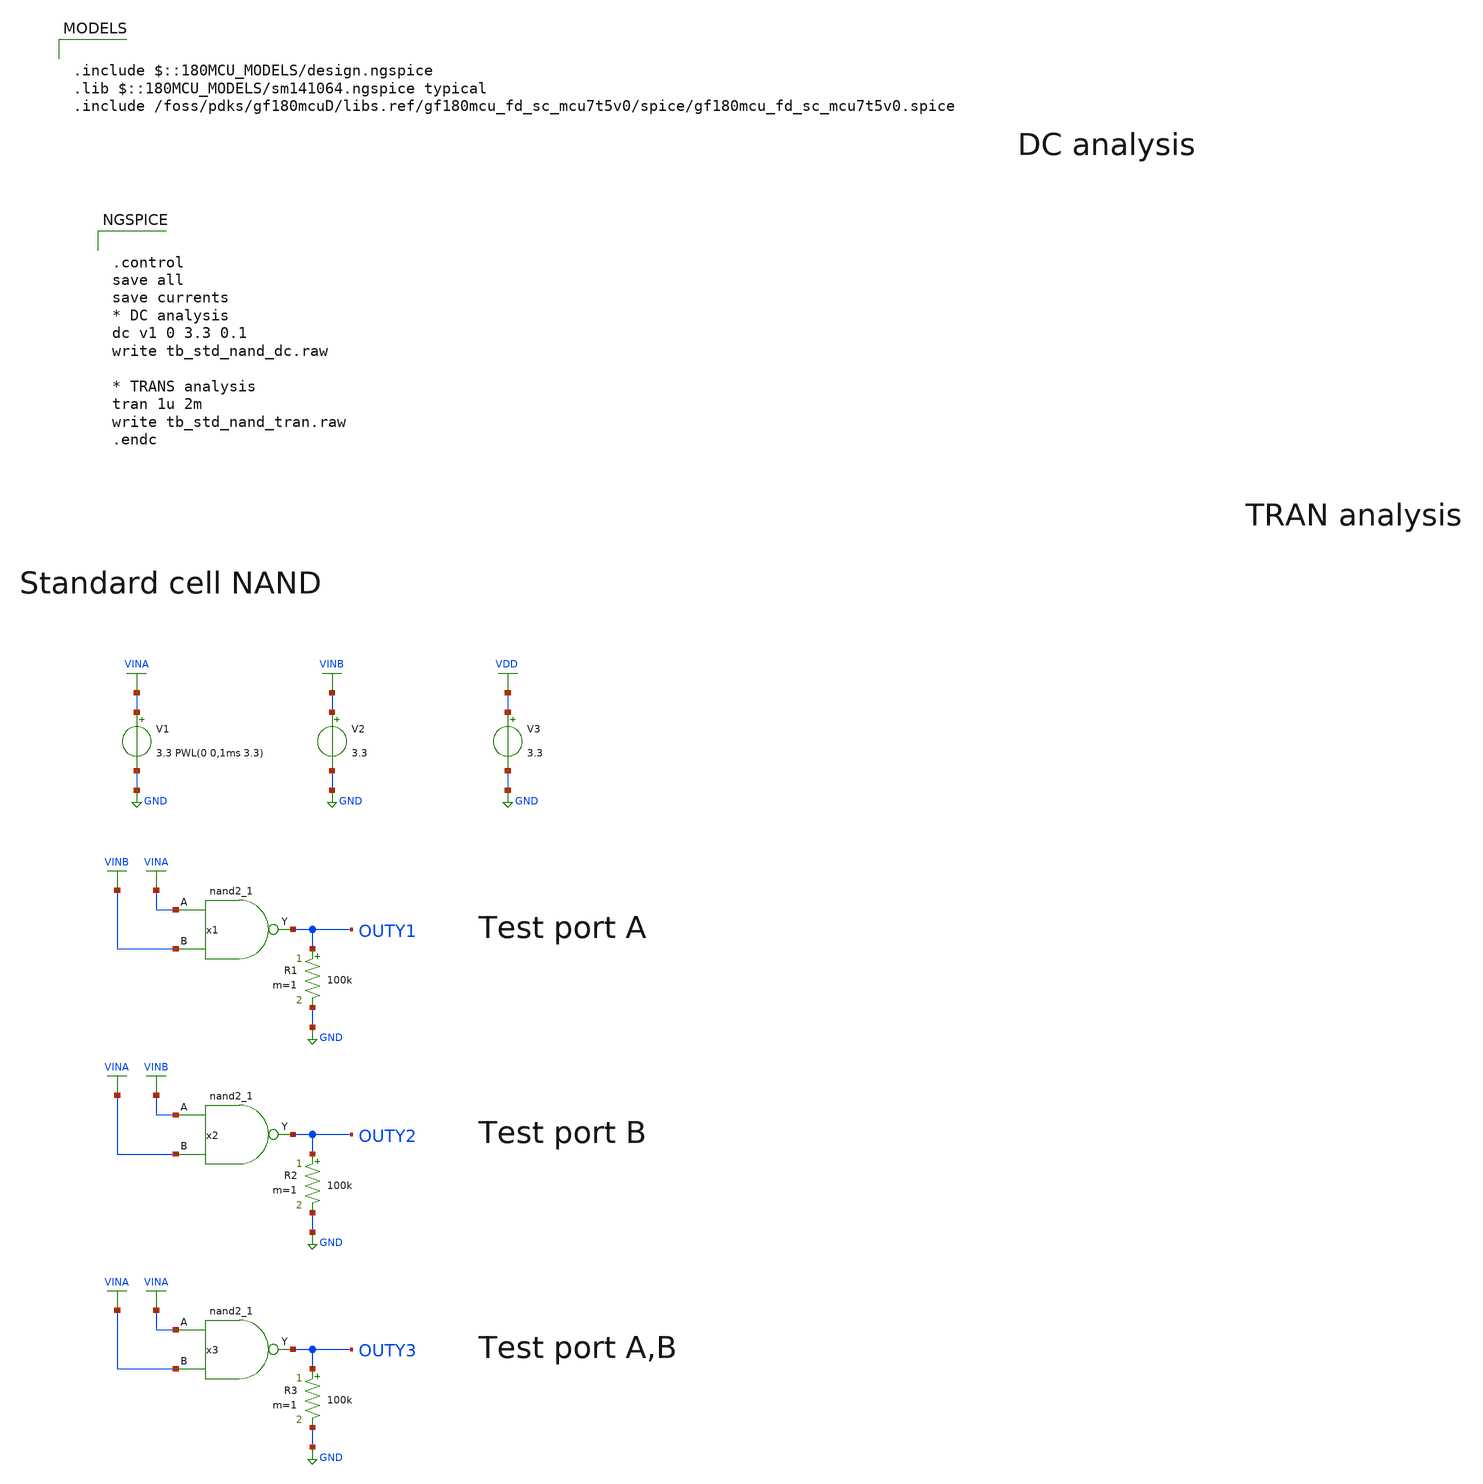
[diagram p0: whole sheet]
** sch_path: designs/libs/tb_analog/tb_std_nand/tb_std_nand.sch
* Copyright 2022 GlobalFoundries PDK Authors
* Licensed under the Apache License, Version 2.0 (the "License");
* you may not use this file except in compliance with the License.
* You may obtain a copy of the License at
* https://www.apache.org/licenses/LICENSE-2.0
* Unless required by applicable law or agreed to in writing, software
* distributed under the License is distributed on an "AS IS" BASIS,
* WITHOUT WARRANTIES OR CONDITIONS OF ANY KIND, either express or implied.
* See the License for the specific language governing permissions and
* limitations under the License.
**.subckt tb_std_nand
V1 VINA GND 3.3 PWL(0 0,1ms 3.3)
x1 VINA VINB OUTY1 VDD VDD GND GND gf180mcu_fd_sc_mcu7t5v0__nand2_1
V2 VINB GND 3.3
V3 VDD GND 3.3
R1 OUTY1 GND 100k m=1
x2 VINB VINA OUTY2 VDD VDD GND GND gf180mcu_fd_sc_mcu7t5v0__nand2_1
R2 OUTY2 GND 100k m=1
x3 VINA VINA OUTY3 VDD VDD GND GND gf180mcu_fd_sc_mcu7t5v0__nand2_1
R3 OUTY3 GND 100k m=1
**** begin user architecture code


.control
save all
save currents
* DC analysis
dc v1 0 3.3 0.1
write tb_std_nand_dc.raw

* TRANS analysis
tran 1u 2m
write tb_std_nand_tran.raw
.endc



.include $::180MCU_MODELS/design.ngspice
.lib $::180MCU_MODELS/sm141064.ngspice typical
.include /foss/pdks/gf180mcuD/libs.ref/gf180mcu_fd_sc_mcu7t5v0/spice/gf180mcu_fd_sc_mcu7t5v0.spice


**** end user architecture code
**.ends
.GLOBAL VDD
.GLOBAL GND
.GLOBAL VINA
.GLOBAL VINB
.end
